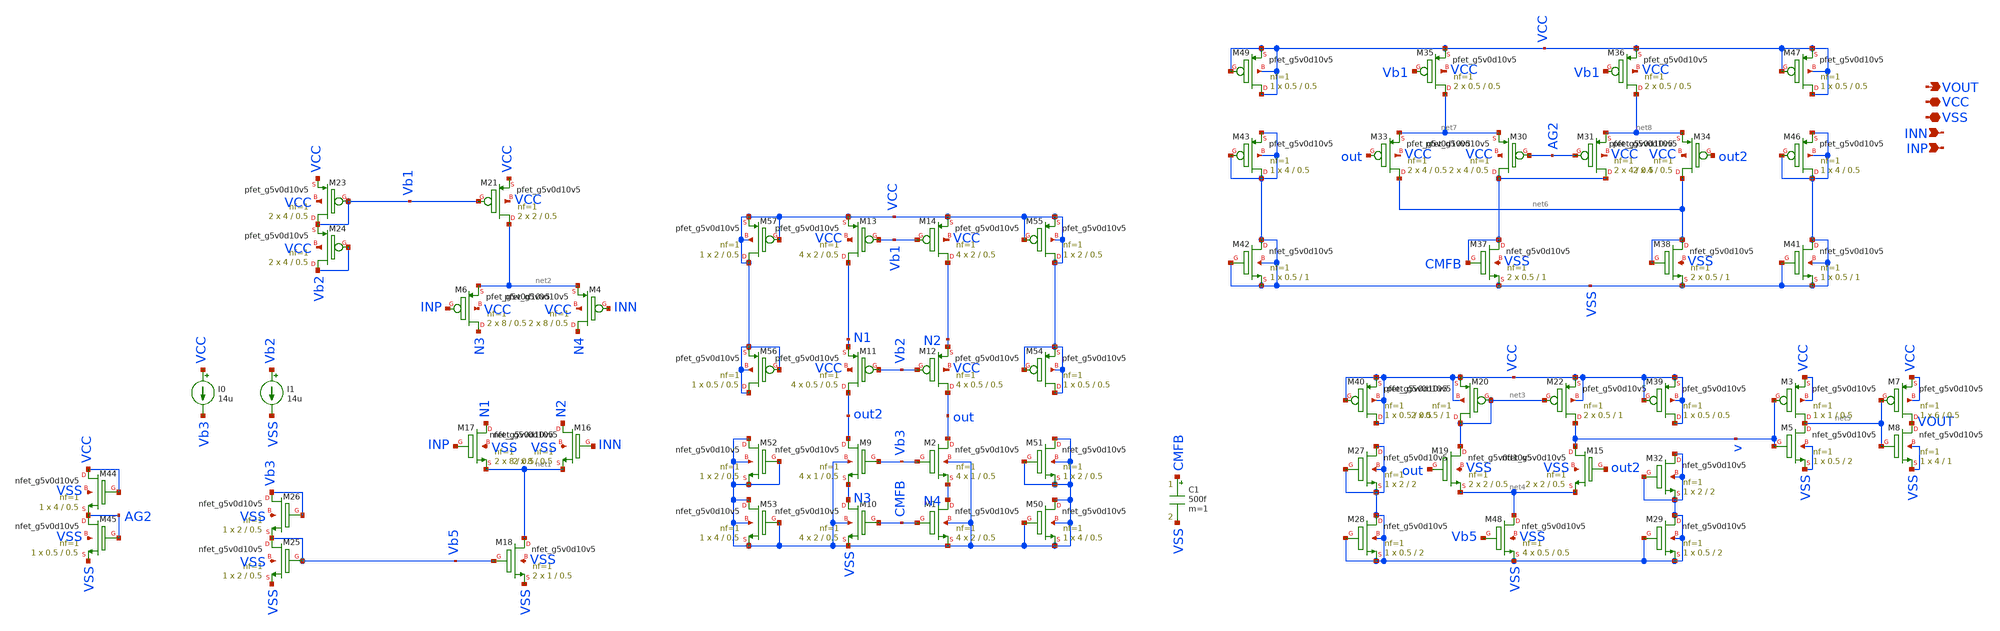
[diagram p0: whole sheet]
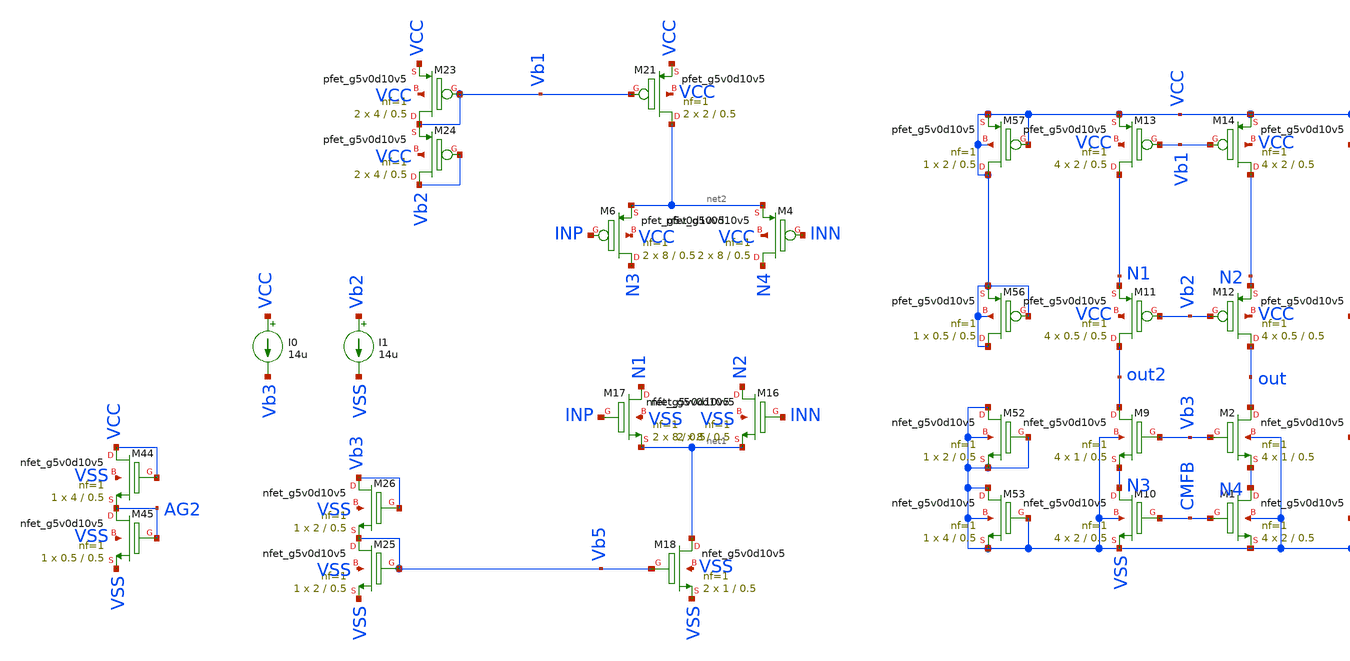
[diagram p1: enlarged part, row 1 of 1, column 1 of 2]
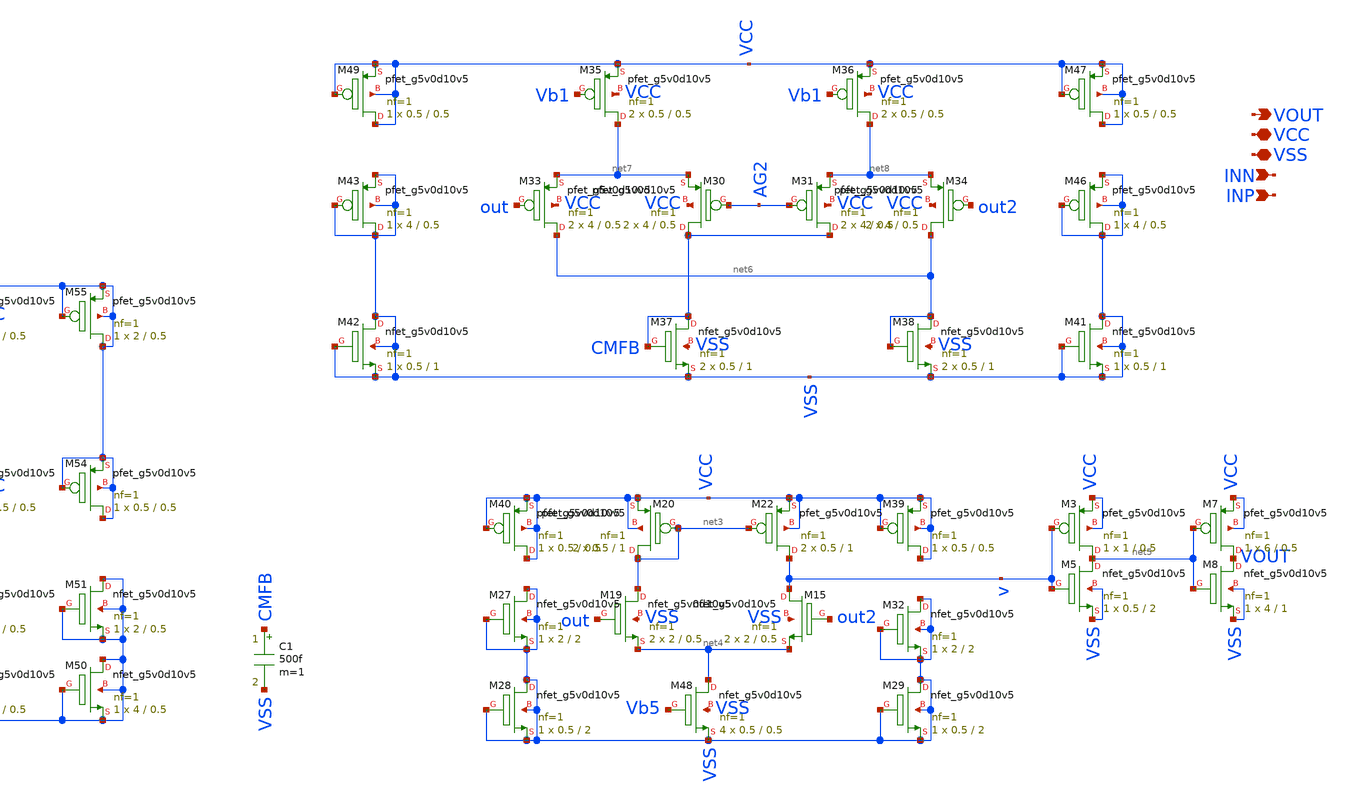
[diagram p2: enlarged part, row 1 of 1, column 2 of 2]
** sch_path: latest_working_comparator/backup_schematic/folded_cascode.sch
**.subckt folded_cascode VOUT VCC VSS INN INP
*.opin VOUT
*.iopin VCC
*.iopin VSS
*.ipin INN
*.ipin INP
XM1 N4 CMFB VSS VSS sky130_fd_pr__nfet_g5v0d10v5 L=0.5 W=2 nf=1 ad='int((nf+1)/2) * W/nf * 0.29' as='int((nf+2)/2) * W/nf * 0.29'
+ pd='2*int((nf+1)/2) * (W/nf + 0.29)' ps='2*int((nf+2)/2) * (W/nf + 0.29)' nrd='0.29 / W' nrs='0.29 / W'
+ sa=0 sb=0 sd=0 mult=4 m=4
XM2 out Vb3 N4 VSS sky130_fd_pr__nfet_g5v0d10v5 L=0.5 W=1 nf=1 ad='int((nf+1)/2) * W/nf * 0.29' as='int((nf+2)/2) * W/nf * 0.29'
+ pd='2*int((nf+1)/2) * (W/nf + 0.29)' ps='2*int((nf+2)/2) * (W/nf + 0.29)' nrd='0.29 / W' nrs='0.29 / W'
+ sa=0 sb=0 sd=0 mult=4 m=4
XM9 out2 Vb3 N3 VSS sky130_fd_pr__nfet_g5v0d10v5 L=0.5 W=1 nf=1 ad='int((nf+1)/2) * W/nf * 0.29' as='int((nf+2)/2) * W/nf * 0.29'
+ pd='2*int((nf+1)/2) * (W/nf + 0.29)' ps='2*int((nf+2)/2) * (W/nf + 0.29)' nrd='0.29 / W' nrs='0.29 / W'
+ sa=0 sb=0 sd=0 mult=4 m=4
XM10 N3 CMFB VSS VSS sky130_fd_pr__nfet_g5v0d10v5 L=0.5 W=2 nf=1 ad='int((nf+1)/2) * W/nf * 0.29' as='int((nf+2)/2) * W/nf * 0.29'
+ pd='2*int((nf+1)/2) * (W/nf + 0.29)' ps='2*int((nf+2)/2) * (W/nf + 0.29)' nrd='0.29 / W' nrs='0.29 / W'
+ sa=0 sb=0 sd=0 mult=4 m=4
XM11 out2 Vb2 N1 VCC sky130_fd_pr__pfet_g5v0d10v5 L=0.5 W=0.5 nf=1 ad='int((nf+1)/2) * W/nf * 0.29' as='int((nf+2)/2) * W/nf * 0.29'
+ pd='2*int((nf+1)/2) * (W/nf + 0.29)' ps='2*int((nf+2)/2) * (W/nf + 0.29)' nrd='0.29 / W' nrs='0.29 / W'
+ sa=0 sb=0 sd=0 mult=4 m=4
XM12 out Vb2 N2 VCC sky130_fd_pr__pfet_g5v0d10v5 L=0.5 W=0.5 nf=1 ad='int((nf+1)/2) * W/nf * 0.29' as='int((nf+2)/2) * W/nf * 0.29'
+ pd='2*int((nf+1)/2) * (W/nf + 0.29)' ps='2*int((nf+2)/2) * (W/nf + 0.29)' nrd='0.29 / W' nrs='0.29 / W'
+ sa=0 sb=0 sd=0 mult=4 m=4
XM13 N1 Vb1 VCC VCC sky130_fd_pr__pfet_g5v0d10v5 L=0.5 W=2 nf=1 ad='int((nf+1)/2) * W/nf * 0.29' as='int((nf+2)/2) * W/nf * 0.29'
+ pd='2*int((nf+1)/2) * (W/nf + 0.29)' ps='2*int((nf+2)/2) * (W/nf + 0.29)' nrd='0.29 / W' nrs='0.29 / W'
+ sa=0 sb=0 sd=0 mult=4 m=4
XM14 N2 Vb1 VCC VCC sky130_fd_pr__pfet_g5v0d10v5 L=0.5 W=2 nf=1 ad='int((nf+1)/2) * W/nf * 0.29' as='int((nf+2)/2) * W/nf * 0.29'
+ pd='2*int((nf+1)/2) * (W/nf + 0.29)' ps='2*int((nf+2)/2) * (W/nf + 0.29)' nrd='0.29 / W' nrs='0.29 / W'
+ sa=0 sb=0 sd=0 mult=4 m=4
XM16 N2 INN net1 VSS sky130_fd_pr__nfet_g5v0d10v5 L=0.5 W=8 nf=1 ad='int((nf+1)/2) * W/nf * 0.29' as='int((nf+2)/2) * W/nf * 0.29'
+ pd='2*int((nf+1)/2) * (W/nf + 0.29)' ps='2*int((nf+2)/2) * (W/nf + 0.29)' nrd='0.29 / W' nrs='0.29 / W'
+ sa=0 sb=0 sd=0 mult=2 m=2
XM17 N1 INP net1 VSS sky130_fd_pr__nfet_g5v0d10v5 L=0.5 W=8 nf=1 ad='int((nf+1)/2) * W/nf * 0.29' as='int((nf+2)/2) * W/nf * 0.29'
+ pd='2*int((nf+1)/2) * (W/nf + 0.29)' ps='2*int((nf+2)/2) * (W/nf + 0.29)' nrd='0.29 / W' nrs='0.29 / W'
+ sa=0 sb=0 sd=0 mult=2 m=2
XM6 N3 INP net2 VCC sky130_fd_pr__pfet_g5v0d10v5 L=0.5 W=8 nf=1 ad='int((nf+1)/2) * W/nf * 0.29' as='int((nf+2)/2) * W/nf * 0.29'
+ pd='2*int((nf+1)/2) * (W/nf + 0.29)' ps='2*int((nf+2)/2) * (W/nf + 0.29)' nrd='0.29 / W' nrs='0.29 / W'
+ sa=0 sb=0 sd=0 mult=2 m=2
XM21 net2 Vb1 VCC VCC sky130_fd_pr__pfet_g5v0d10v5 L=0.5 W=2 nf=1 ad='int((nf+1)/2) * W/nf * 0.29' as='int((nf+2)/2) * W/nf * 0.29'
+ pd='2*int((nf+1)/2) * (W/nf + 0.29)' ps='2*int((nf+2)/2) * (W/nf + 0.29)' nrd='0.29 / W' nrs='0.29 / W'
+ sa=0 sb=0 sd=0 mult=2 m=2
XM23 Vb1 Vb1 VCC VCC sky130_fd_pr__pfet_g5v0d10v5 L=0.5 W=4 nf=1 ad='int((nf+1)/2) * W/nf * 0.29' as='int((nf+2)/2) * W/nf * 0.29'
+ pd='2*int((nf+1)/2) * (W/nf + 0.29)' ps='2*int((nf+2)/2) * (W/nf + 0.29)' nrd='0.29 / W' nrs='0.29 / W'
+ sa=0 sb=0 sd=0 mult=2 m=2
XM24 Vb2 Vb2 Vb1 VCC sky130_fd_pr__pfet_g5v0d10v5 L=0.5 W=4 nf=1 ad='int((nf+1)/2) * W/nf * 0.29' as='int((nf+2)/2) * W/nf * 0.29'
+ pd='2*int((nf+1)/2) * (W/nf + 0.29)' ps='2*int((nf+2)/2) * (W/nf + 0.29)' nrd='0.29 / W' nrs='0.29 / W'
+ sa=0 sb=0 sd=0 mult=2 m=2
XM25 Vb5 Vb5 VSS VSS sky130_fd_pr__nfet_g5v0d10v5 L=0.5 W=2 nf=1 ad='int((nf+1)/2) * W/nf * 0.29' as='int((nf+2)/2) * W/nf * 0.29'
+ pd='2*int((nf+1)/2) * (W/nf + 0.29)' ps='2*int((nf+2)/2) * (W/nf + 0.29)' nrd='0.29 / W' nrs='0.29 / W'
+ sa=0 sb=0 sd=0 mult=1 m=1
XM26 Vb3 Vb3 Vb5 VSS sky130_fd_pr__nfet_g5v0d10v5 L=0.5 W=2 nf=1 ad='int((nf+1)/2) * W/nf * 0.29' as='int((nf+2)/2) * W/nf * 0.29'
+ pd='2*int((nf+1)/2) * (W/nf + 0.29)' ps='2*int((nf+2)/2) * (W/nf + 0.29)' nrd='0.29 / W' nrs='0.29 / W'
+ sa=0 sb=0 sd=0 mult=1 m=1
XM18 net1 Vb5 VSS VSS sky130_fd_pr__nfet_g5v0d10v5 L=0.5 W=1 nf=1 ad='int((nf+1)/2) * W/nf * 0.29' as='int((nf+2)/2) * W/nf * 0.29'
+ pd='2*int((nf+1)/2) * (W/nf + 0.29)' ps='2*int((nf+2)/2) * (W/nf + 0.29)' nrd='0.29 / W' nrs='0.29 / W'
+ sa=0 sb=0 sd=0 mult=2 m=2
XM44 VCC VCC AG2 VSS sky130_fd_pr__nfet_g5v0d10v5 L=0.5 W=4 nf=1 ad='int((nf+1)/2) * W/nf * 0.29' as='int((nf+2)/2) * W/nf * 0.29'
+ pd='2*int((nf+1)/2) * (W/nf + 0.29)' ps='2*int((nf+2)/2) * (W/nf + 0.29)' nrd='0.29 / W' nrs='0.29 / W'
+ sa=0 sb=0 sd=0 mult=1 m=1
XM45 AG2 AG2 VSS VSS sky130_fd_pr__nfet_g5v0d10v5 L=0.5 W=0.5 nf=1 ad='int((nf+1)/2) * W/nf * 0.29' as='int((nf+2)/2) * W/nf * 0.29'
+ pd='2*int((nf+1)/2) * (W/nf + 0.29)' ps='2*int((nf+2)/2) * (W/nf + 0.29)' nrd='0.29 / W' nrs='0.29 / W'
+ sa=0 sb=0 sd=0 mult=1 m=1
C1 CMFB VSS 500f m=1
XM4 N4 INN net2 VCC sky130_fd_pr__pfet_g5v0d10v5 L=0.5 W=8 nf=1 ad='int((nf+1)/2) * W/nf * 0.29' as='int((nf+2)/2) * W/nf * 0.29'
+ pd='2*int((nf+1)/2) * (W/nf + 0.29)' ps='2*int((nf+2)/2) * (W/nf + 0.29)' nrd='0.29 / W' nrs='0.29 / W'
+ sa=0 sb=0 sd=0 mult=2 m=2
I0 VCC Vb3 14u
I1 Vb2 VSS 14u
XM20 net3 net3 VCC VCC sky130_fd_pr__pfet_g5v0d10v5 L=1 W=0.5 nf=1 ad='int((nf+1)/2) * W/nf * 0.29' as='int((nf+2)/2) * W/nf * 0.29'
+ pd='2*int((nf+1)/2) * (W/nf + 0.29)' ps='2*int((nf+2)/2) * (W/nf + 0.29)' nrd='0.29 / W' nrs='0.29 / W'
+ sa=0 sb=0 sd=0 mult=2 m=2
XM22 v net3 VCC VCC sky130_fd_pr__pfet_g5v0d10v5 L=1 W=0.5 nf=1 ad='int((nf+1)/2) * W/nf * 0.29' as='int((nf+2)/2) * W/nf * 0.29'
+ pd='2*int((nf+1)/2) * (W/nf + 0.29)' ps='2*int((nf+2)/2) * (W/nf + 0.29)' nrd='0.29 / W' nrs='0.29 / W'
+ sa=0 sb=0 sd=0 mult=2 m=2
XM15 v out2 net4 VSS sky130_fd_pr__nfet_g5v0d10v5 L=0.5 W=2 nf=1 ad='int((nf+1)/2) * W/nf * 0.29' as='int((nf+2)/2) * W/nf * 0.29'
+ pd='2*int((nf+1)/2) * (W/nf + 0.29)' ps='2*int((nf+2)/2) * (W/nf + 0.29)' nrd='0.29 / W' nrs='0.29 / W'
+ sa=0 sb=0 sd=0 mult=2 m=2
XM19 net3 out net4 VSS sky130_fd_pr__nfet_g5v0d10v5 L=0.5 W=2 nf=1 ad='int((nf+1)/2) * W/nf * 0.29' as='int((nf+2)/2) * W/nf * 0.29'
+ pd='2*int((nf+1)/2) * (W/nf + 0.29)' ps='2*int((nf+2)/2) * (W/nf + 0.29)' nrd='0.29 / W' nrs='0.29 / W'
+ sa=0 sb=0 sd=0 mult=2 m=2
XM48 net4 Vb5 VSS VSS sky130_fd_pr__nfet_g5v0d10v5 L=0.5 W=0.5 nf=1 ad='int((nf+1)/2) * W/nf * 0.29'
+ as='int((nf+2)/2) * W/nf * 0.29' pd='2*int((nf+1)/2) * (W/nf + 0.29)' ps='2*int((nf+2)/2) * (W/nf + 0.29)'
+ nrd='0.29 / W' nrs='0.29 / W' sa=0 sb=0 sd=0 mult=4 m=4
XM3 net5 v VCC VCC sky130_fd_pr__pfet_g5v0d10v5 L=0.5 W=1 nf=1 ad='int((nf+1)/2) * W/nf * 0.29' as='int((nf+2)/2) * W/nf * 0.29'
+ pd='2*int((nf+1)/2) * (W/nf + 0.29)' ps='2*int((nf+2)/2) * (W/nf + 0.29)' nrd='0.29 / W' nrs='0.29 / W'
+ sa=0 sb=0 sd=0 mult=1 m=1
XM5 net5 v VSS VSS sky130_fd_pr__nfet_g5v0d10v5 L=2 W=0.5 nf=1 ad='int((nf+1)/2) * W/nf * 0.29' as='int((nf+2)/2) * W/nf * 0.29'
+ pd='2*int((nf+1)/2) * (W/nf + 0.29)' ps='2*int((nf+2)/2) * (W/nf + 0.29)' nrd='0.29 / W' nrs='0.29 / W'
+ sa=0 sb=0 sd=0 mult=1 m=1
XM7 VOUT net5 VCC VCC sky130_fd_pr__pfet_g5v0d10v5 L=0.5 W=6 nf=1 ad='int((nf+1)/2) * W/nf * 0.29' as='int((nf+2)/2) * W/nf * 0.29'
+ pd='2*int((nf+1)/2) * (W/nf + 0.29)' ps='2*int((nf+2)/2) * (W/nf + 0.29)' nrd='0.29 / W' nrs='0.29 / W'
+ sa=0 sb=0 sd=0 mult=1 m=1
XM8 VOUT net5 VSS VSS sky130_fd_pr__nfet_g5v0d10v5 L=1 W=4 nf=1 ad='int((nf+1)/2) * W/nf * 0.29' as='int((nf+2)/2) * W/nf * 0.29'
+ pd='2*int((nf+1)/2) * (W/nf + 0.29)' ps='2*int((nf+2)/2) * (W/nf + 0.29)' nrd='0.29 / W' nrs='0.29 / W'
+ sa=0 sb=0 sd=0 mult=1 m=1
XM27 VSS VSS VSS VSS sky130_fd_pr__nfet_g5v0d10v5 L=2 W=2 nf=1 ad='int((nf+1)/2) * W/nf * 0.29' as='int((nf+2)/2) * W/nf * 0.29'
+ pd='2*int((nf+1)/2) * (W/nf + 0.29)' ps='2*int((nf+2)/2) * (W/nf + 0.29)' nrd='0.29 / W' nrs='0.29 / W'
+ sa=0 sb=0 sd=0 mult=1 m=1
XM28 VSS VSS VSS VSS sky130_fd_pr__nfet_g5v0d10v5 L=2 W=0.5 nf=1 ad='int((nf+1)/2) * W/nf * 0.29' as='int((nf+2)/2) * W/nf * 0.29'
+ pd='2*int((nf+1)/2) * (W/nf + 0.29)' ps='2*int((nf+2)/2) * (W/nf + 0.29)' nrd='0.29 / W' nrs='0.29 / W'
+ sa=0 sb=0 sd=0 mult=1 m=1
XM29 VSS VSS VSS VSS sky130_fd_pr__nfet_g5v0d10v5 L=2 W=0.5 nf=1 ad='int((nf+1)/2) * W/nf * 0.29' as='int((nf+2)/2) * W/nf * 0.29'
+ pd='2*int((nf+1)/2) * (W/nf + 0.29)' ps='2*int((nf+2)/2) * (W/nf + 0.29)' nrd='0.29 / W' nrs='0.29 / W'
+ sa=0 sb=0 sd=0 mult=1 m=1
XM32 VSS VSS VSS VSS sky130_fd_pr__nfet_g5v0d10v5 L=2 W=2 nf=1 ad='int((nf+1)/2) * W/nf * 0.29' as='int((nf+2)/2) * W/nf * 0.29'
+ pd='2*int((nf+1)/2) * (W/nf + 0.29)' ps='2*int((nf+2)/2) * (W/nf + 0.29)' nrd='0.29 / W' nrs='0.29 / W'
+ sa=0 sb=0 sd=0 mult=1 m=1
XM39 VCC VCC VCC VCC sky130_fd_pr__pfet_g5v0d10v5 L=0.5 W=0.5 nf=1 ad='int((nf+1)/2) * W/nf * 0.29' as='int((nf+2)/2) * W/nf * 0.29'
+ pd='2*int((nf+1)/2) * (W/nf + 0.29)' ps='2*int((nf+2)/2) * (W/nf + 0.29)' nrd='0.29 / W' nrs='0.29 / W'
+ sa=0 sb=0 sd=0 mult=1 m=1
XM40 VCC VCC VCC VCC sky130_fd_pr__pfet_g5v0d10v5 L=0.5 W=0.5 nf=1 ad='int((nf+1)/2) * W/nf * 0.29' as='int((nf+2)/2) * W/nf * 0.29'
+ pd='2*int((nf+1)/2) * (W/nf + 0.29)' ps='2*int((nf+2)/2) * (W/nf + 0.29)' nrd='0.29 / W' nrs='0.29 / W'
+ sa=0 sb=0 sd=0 mult=1 m=1
XM30 CMFB AG2 net7 VCC sky130_fd_pr__pfet_g5v0d10v5 L=0.5 W=4 nf=1 ad='int((nf+1)/2) * W/nf * 0.29' as='int((nf+2)/2) * W/nf * 0.29'
+ pd='2*int((nf+1)/2) * (W/nf + 0.29)' ps='2*int((nf+2)/2) * (W/nf + 0.29)' nrd='0.29 / W' nrs='0.29 / W'
+ sa=0 sb=0 sd=0 mult=2 m=2
XM31 CMFB AG2 net8 VCC sky130_fd_pr__pfet_g5v0d10v5 L=0.5 W=4 nf=1 ad='int((nf+1)/2) * W/nf * 0.29' as='int((nf+2)/2) * W/nf * 0.29'
+ pd='2*int((nf+1)/2) * (W/nf + 0.29)' ps='2*int((nf+2)/2) * (W/nf + 0.29)' nrd='0.29 / W' nrs='0.29 / W'
+ sa=0 sb=0 sd=0 mult=2 m=2
XM33 net6 out net7 VCC sky130_fd_pr__pfet_g5v0d10v5 L=0.5 W=4 nf=1 ad='int((nf+1)/2) * W/nf * 0.29' as='int((nf+2)/2) * W/nf * 0.29'
+ pd='2*int((nf+1)/2) * (W/nf + 0.29)' ps='2*int((nf+2)/2) * (W/nf + 0.29)' nrd='0.29 / W' nrs='0.29 / W'
+ sa=0 sb=0 sd=0 mult=2 m=2
XM34 net6 out2 net8 VCC sky130_fd_pr__pfet_g5v0d10v5 L=0.5 W=4 nf=1 ad='int((nf+1)/2) * W/nf * 0.29'
+ as='int((nf+2)/2) * W/nf * 0.29' pd='2*int((nf+1)/2) * (W/nf + 0.29)' ps='2*int((nf+2)/2) * (W/nf + 0.29)'
+ nrd='0.29 / W' nrs='0.29 / W' sa=0 sb=0 sd=0 mult=2 m=2
XM35 net7 Vb1 VCC VCC sky130_fd_pr__pfet_g5v0d10v5 L=0.5 W=0.5 nf=1 ad='int((nf+1)/2) * W/nf * 0.29'
+ as='int((nf+2)/2) * W/nf * 0.29' pd='2*int((nf+1)/2) * (W/nf + 0.29)' ps='2*int((nf+2)/2) * (W/nf + 0.29)'
+ nrd='0.29 / W' nrs='0.29 / W' sa=0 sb=0 sd=0 mult=2 m=2
XM36 net8 Vb1 VCC VCC sky130_fd_pr__pfet_g5v0d10v5 L=0.5 W=0.5 nf=1 ad='int((nf+1)/2) * W/nf * 0.29'
+ as='int((nf+2)/2) * W/nf * 0.29' pd='2*int((nf+1)/2) * (W/nf + 0.29)' ps='2*int((nf+2)/2) * (W/nf + 0.29)'
+ nrd='0.29 / W' nrs='0.29 / W' sa=0 sb=0 sd=0 mult=2 m=2
XM37 CMFB CMFB VSS VSS sky130_fd_pr__nfet_g5v0d10v5 L=1 W=0.5 nf=1 ad='int((nf+1)/2) * W/nf * 0.29' as='int((nf+2)/2) * W/nf * 0.29'
+ pd='2*int((nf+1)/2) * (W/nf + 0.29)' ps='2*int((nf+2)/2) * (W/nf + 0.29)' nrd='0.29 / W' nrs='0.29 / W'
+ sa=0 sb=0 sd=0 mult=2 m=2
XM38 net6 net6 VSS VSS sky130_fd_pr__nfet_g5v0d10v5 L=1 W=0.5 nf=1 ad='int((nf+1)/2) * W/nf * 0.29' as='int((nf+2)/2) * W/nf * 0.29'
+ pd='2*int((nf+1)/2) * (W/nf + 0.29)' ps='2*int((nf+2)/2) * (W/nf + 0.29)' nrd='0.29 / W' nrs='0.29 / W'
+ sa=0 sb=0 sd=0 mult=2 m=2
XM41 VSS VSS VSS VSS sky130_fd_pr__nfet_g5v0d10v5 L=1 W=0.5 nf=1 ad='int((nf+1)/2) * W/nf * 0.29' as='int((nf+2)/2) * W/nf * 0.29'
+ pd='2*int((nf+1)/2) * (W/nf + 0.29)' ps='2*int((nf+2)/2) * (W/nf + 0.29)' nrd='0.29 / W' nrs='0.29 / W'
+ sa=0 sb=0 sd=0 mult=1 m=1
XM42 VSS VSS VSS VSS sky130_fd_pr__nfet_g5v0d10v5 L=1 W=0.5 nf=1 ad='int((nf+1)/2) * W/nf * 0.29' as='int((nf+2)/2) * W/nf * 0.29'
+ pd='2*int((nf+1)/2) * (W/nf + 0.29)' ps='2*int((nf+2)/2) * (W/nf + 0.29)' nrd='0.29 / W' nrs='0.29 / W'
+ sa=0 sb=0 sd=0 mult=1 m=1
XM43 VSS VSS VSS VSS sky130_fd_pr__pfet_g5v0d10v5 L=0.5 W=4 nf=1 ad='int((nf+1)/2) * W/nf * 0.29' as='int((nf+2)/2) * W/nf * 0.29'
+ pd='2*int((nf+1)/2) * (W/nf + 0.29)' ps='2*int((nf+2)/2) * (W/nf + 0.29)' nrd='0.29 / W' nrs='0.29 / W'
+ sa=0 sb=0 sd=0 mult=1 m=1
XM47 VCC VCC VCC VCC sky130_fd_pr__pfet_g5v0d10v5 L=0.5 W=0.5 nf=1 ad='int((nf+1)/2) * W/nf * 0.29' as='int((nf+2)/2) * W/nf * 0.29'
+ pd='2*int((nf+1)/2) * (W/nf + 0.29)' ps='2*int((nf+2)/2) * (W/nf + 0.29)' nrd='0.29 / W' nrs='0.29 / W'
+ sa=0 sb=0 sd=0 mult=1 m=1
XM49 VCC VCC VCC VCC sky130_fd_pr__pfet_g5v0d10v5 L=0.5 W=0.5 nf=1 ad='int((nf+1)/2) * W/nf * 0.29' as='int((nf+2)/2) * W/nf * 0.29'
+ pd='2*int((nf+1)/2) * (W/nf + 0.29)' ps='2*int((nf+2)/2) * (W/nf + 0.29)' nrd='0.29 / W' nrs='0.29 / W'
+ sa=0 sb=0 sd=0 mult=1 m=1
XM46 VSS VSS VSS VSS sky130_fd_pr__pfet_g5v0d10v5 L=0.5 W=4 nf=1 ad='int((nf+1)/2) * W/nf * 0.29' as='int((nf+2)/2) * W/nf * 0.29'
+ pd='2*int((nf+1)/2) * (W/nf + 0.29)' ps='2*int((nf+2)/2) * (W/nf + 0.29)' nrd='0.29 / W' nrs='0.29 / W'
+ sa=0 sb=0 sd=0 mult=1 m=1
XM50 VSS VSS VSS VSS sky130_fd_pr__nfet_g5v0d10v5 L=0.5 W=4 nf=1 ad='int((nf+1)/2) * W/nf * 0.29' as='int((nf+2)/2) * W/nf * 0.29'
+ pd='2*int((nf+1)/2) * (W/nf + 0.29)' ps='2*int((nf+2)/2) * (W/nf + 0.29)' nrd='0.29 / W' nrs='0.29 / W'
+ sa=0 sb=0 sd=0 mult=1 m=1
XM51 VSS VSS VSS VSS sky130_fd_pr__nfet_g5v0d10v5 L=0.5 W=2 nf=1 ad='int((nf+1)/2) * W/nf * 0.29' as='int((nf+2)/2) * W/nf * 0.29'
+ pd='2*int((nf+1)/2) * (W/nf + 0.29)' ps='2*int((nf+2)/2) * (W/nf + 0.29)' nrd='0.29 / W' nrs='0.29 / W'
+ sa=0 sb=0 sd=0 mult=1 m=1
XM52 VSS VSS VSS VSS sky130_fd_pr__nfet_g5v0d10v5 L=0.5 W=2 nf=1 ad='int((nf+1)/2) * W/nf * 0.29' as='int((nf+2)/2) * W/nf * 0.29'
+ pd='2*int((nf+1)/2) * (W/nf + 0.29)' ps='2*int((nf+2)/2) * (W/nf + 0.29)' nrd='0.29 / W' nrs='0.29 / W'
+ sa=0 sb=0 sd=0 mult=1 m=1
XM53 VSS VSS VSS VSS sky130_fd_pr__nfet_g5v0d10v5 L=0.5 W=4 nf=1 ad='int((nf+1)/2) * W/nf * 0.29' as='int((nf+2)/2) * W/nf * 0.29'
+ pd='2*int((nf+1)/2) * (W/nf + 0.29)' ps='2*int((nf+2)/2) * (W/nf + 0.29)' nrd='0.29 / W' nrs='0.29 / W'
+ sa=0 sb=0 sd=0 mult=1 m=1
XM54 VCC VCC VCC VCC sky130_fd_pr__pfet_g5v0d10v5 L=0.5 W=0.5 nf=1 ad='int((nf+1)/2) * W/nf * 0.29' as='int((nf+2)/2) * W/nf * 0.29'
+ pd='2*int((nf+1)/2) * (W/nf + 0.29)' ps='2*int((nf+2)/2) * (W/nf + 0.29)' nrd='0.29 / W' nrs='0.29 / W'
+ sa=0 sb=0 sd=0 mult=1 m=1
XM55 VCC VCC VCC VCC sky130_fd_pr__pfet_g5v0d10v5 L=0.5 W=2 nf=1 ad='int((nf+1)/2) * W/nf * 0.29' as='int((nf+2)/2) * W/nf * 0.29'
+ pd='2*int((nf+1)/2) * (W/nf + 0.29)' ps='2*int((nf+2)/2) * (W/nf + 0.29)' nrd='0.29 / W' nrs='0.29 / W'
+ sa=0 sb=0 sd=0 mult=1 m=1
XM56 VCC VCC VCC VCC sky130_fd_pr__pfet_g5v0d10v5 L=0.5 W=0.5 nf=1 ad='int((nf+1)/2) * W/nf * 0.29' as='int((nf+2)/2) * W/nf * 0.29'
+ pd='2*int((nf+1)/2) * (W/nf + 0.29)' ps='2*int((nf+2)/2) * (W/nf + 0.29)' nrd='0.29 / W' nrs='0.29 / W'
+ sa=0 sb=0 sd=0 mult=1 m=1
XM57 VCC VCC VCC VCC sky130_fd_pr__pfet_g5v0d10v5 L=0.5 W=2 nf=1 ad='int((nf+1)/2) * W/nf * 0.29' as='int((nf+2)/2) * W/nf * 0.29'
+ pd='2*int((nf+1)/2) * (W/nf + 0.29)' ps='2*int((nf+2)/2) * (W/nf + 0.29)' nrd='0.29 / W' nrs='0.29 / W'
+ sa=0 sb=0 sd=0 mult=1 m=1
**.ends
.end
